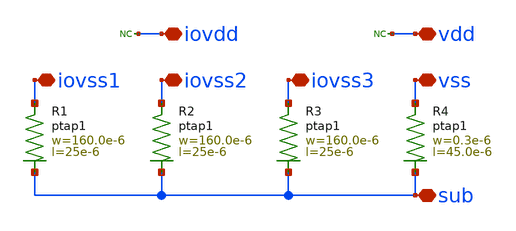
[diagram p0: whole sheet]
** sch_path: MSPHY6034-main/schematic/xschem/openpdk-libraries/ihp-sg13g2/sg13g2_io/xschem/sg13g2_Corner.sch
**.subckt sg13g2_Corner vss iovdd vdd sub iovss1 iovss2 iovss3
*.iopin vss
*.iopin iovdd
*.iopin vdd
*.iopin sub
*.iopin iovss1
*.iopin iovss2
*.iopin iovss3
XR3 iovss3 sub ptap1 R=224.3m w=160.0e-6 l=25e-6
XR4 vss sub ptap1 R=9.414 w=0.3e-6 l=45.0e-6
* noconn iovdd
* noconn vdd
XR1 iovss1 sub ptap1 R=224.3m w=160.0e-6 l=25e-6
XR2 iovss2 sub ptap1 R=224.3m w=160.0e-6 l=25e-6
**.ends
.end
